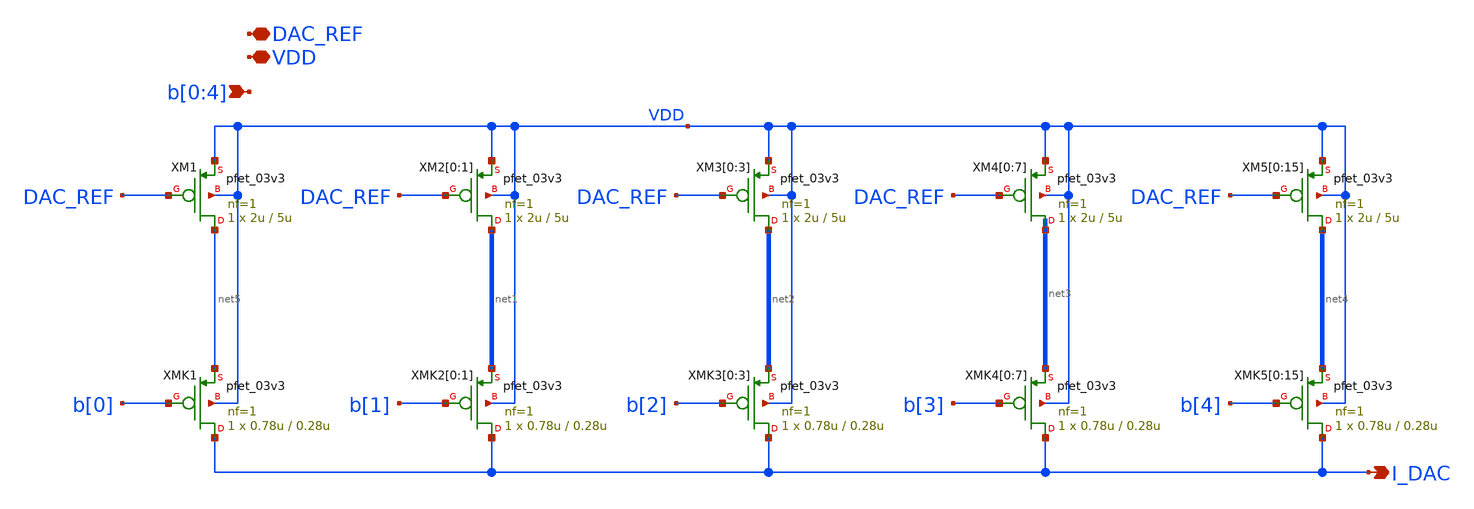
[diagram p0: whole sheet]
** sch_path: DAC_CORE_5bit/DAC_CORE_5bit.sch
**.subckt DAC_CORE_5bit I_DAC VDD DAC_REF b[0],b[1],b[2],b[3],b[4]
*.opin I_DAC
*.iopin VDD
*.iopin DAC_REF
*.ipin b[0],b[1],b[2],b[3],b[4]
XMK1 I_DAC b[0] net5 VDD pfet_03v3 L=0.28u W=0.78u nf=1 ad='int((nf+1)/2) * W/nf * 0.18u' as='int((nf+2)/2) * W/nf * 0.18u'
+ pd='2*int((nf+1)/2) * (W/nf + 0.18u)' ps='2*int((nf+2)/2) * (W/nf + 0.18u)' nrd='0.18u / W' nrs='0.18u / W'
+ sa=0 sb=0 sd=0 m=1
XMK2[0] I_DAC b[1] net1[1] VDD pfet_03v3 L=0.28u W=0.78u nf=1 ad='int((nf+1)/2) * W/nf * 0.18u' as='int((nf+2)/2) * W/nf * 0.18u'
+ pd='2*int((nf+1)/2) * (W/nf + 0.18u)' ps='2*int((nf+2)/2) * (W/nf + 0.18u)' nrd='0.18u / W' nrs='0.18u / W'
+ sa=0 sb=0 sd=0 m=1
XMK2[1] I_DAC b[1] net1[0] VDD pfet_03v3 L=0.28u W=0.78u nf=1 ad='int((nf+1)/2) * W/nf * 0.18u' as='int((nf+2)/2) * W/nf * 0.18u'
+ pd='2*int((nf+1)/2) * (W/nf + 0.18u)' ps='2*int((nf+2)/2) * (W/nf + 0.18u)' nrd='0.18u / W' nrs='0.18u / W'
+ sa=0 sb=0 sd=0 m=1
XMK3[0] I_DAC b[2] net2[3] VDD pfet_03v3 L=0.28u W=0.78u nf=1 ad='int((nf+1)/2) * W/nf * 0.18u' as='int((nf+2)/2) * W/nf * 0.18u'
+ pd='2*int((nf+1)/2) * (W/nf + 0.18u)' ps='2*int((nf+2)/2) * (W/nf + 0.18u)' nrd='0.18u / W' nrs='0.18u / W'
+ sa=0 sb=0 sd=0 m=1
XMK3[1] I_DAC b[2] net2[2] VDD pfet_03v3 L=0.28u W=0.78u nf=1 ad='int((nf+1)/2) * W/nf * 0.18u' as='int((nf+2)/2) * W/nf * 0.18u'
+ pd='2*int((nf+1)/2) * (W/nf + 0.18u)' ps='2*int((nf+2)/2) * (W/nf + 0.18u)' nrd='0.18u / W' nrs='0.18u / W'
+ sa=0 sb=0 sd=0 m=1
XMK3[2] I_DAC b[2] net2[1] VDD pfet_03v3 L=0.28u W=0.78u nf=1 ad='int((nf+1)/2) * W/nf * 0.18u' as='int((nf+2)/2) * W/nf * 0.18u'
+ pd='2*int((nf+1)/2) * (W/nf + 0.18u)' ps='2*int((nf+2)/2) * (W/nf + 0.18u)' nrd='0.18u / W' nrs='0.18u / W'
+ sa=0 sb=0 sd=0 m=1
XMK3[3] I_DAC b[2] net2[0] VDD pfet_03v3 L=0.28u W=0.78u nf=1 ad='int((nf+1)/2) * W/nf * 0.18u' as='int((nf+2)/2) * W/nf * 0.18u'
+ pd='2*int((nf+1)/2) * (W/nf + 0.18u)' ps='2*int((nf+2)/2) * (W/nf + 0.18u)' nrd='0.18u / W' nrs='0.18u / W'
+ sa=0 sb=0 sd=0 m=1
XMK4[0] I_DAC b[3] net3[7] VDD pfet_03v3 L=0.28u W=0.78u nf=1 ad='int((nf+1)/2) * W/nf * 0.18u' as='int((nf+2)/2) * W/nf * 0.18u'
+ pd='2*int((nf+1)/2) * (W/nf + 0.18u)' ps='2*int((nf+2)/2) * (W/nf + 0.18u)' nrd='0.18u / W' nrs='0.18u / W'
+ sa=0 sb=0 sd=0 m=1
XMK4[1] I_DAC b[3] net3[6] VDD pfet_03v3 L=0.28u W=0.78u nf=1 ad='int((nf+1)/2) * W/nf * 0.18u' as='int((nf+2)/2) * W/nf * 0.18u'
+ pd='2*int((nf+1)/2) * (W/nf + 0.18u)' ps='2*int((nf+2)/2) * (W/nf + 0.18u)' nrd='0.18u / W' nrs='0.18u / W'
+ sa=0 sb=0 sd=0 m=1
XMK4[2] I_DAC b[3] net3[5] VDD pfet_03v3 L=0.28u W=0.78u nf=1 ad='int((nf+1)/2) * W/nf * 0.18u' as='int((nf+2)/2) * W/nf * 0.18u'
+ pd='2*int((nf+1)/2) * (W/nf + 0.18u)' ps='2*int((nf+2)/2) * (W/nf + 0.18u)' nrd='0.18u / W' nrs='0.18u / W'
+ sa=0 sb=0 sd=0 m=1
XMK4[3] I_DAC b[3] net3[4] VDD pfet_03v3 L=0.28u W=0.78u nf=1 ad='int((nf+1)/2) * W/nf * 0.18u' as='int((nf+2)/2) * W/nf * 0.18u'
+ pd='2*int((nf+1)/2) * (W/nf + 0.18u)' ps='2*int((nf+2)/2) * (W/nf + 0.18u)' nrd='0.18u / W' nrs='0.18u / W'
+ sa=0 sb=0 sd=0 m=1
XMK4[4] I_DAC b[3] net3[3] VDD pfet_03v3 L=0.28u W=0.78u nf=1 ad='int((nf+1)/2) * W/nf * 0.18u' as='int((nf+2)/2) * W/nf * 0.18u'
+ pd='2*int((nf+1)/2) * (W/nf + 0.18u)' ps='2*int((nf+2)/2) * (W/nf + 0.18u)' nrd='0.18u / W' nrs='0.18u / W'
+ sa=0 sb=0 sd=0 m=1
XMK4[5] I_DAC b[3] net3[2] VDD pfet_03v3 L=0.28u W=0.78u nf=1 ad='int((nf+1)/2) * W/nf * 0.18u' as='int((nf+2)/2) * W/nf * 0.18u'
+ pd='2*int((nf+1)/2) * (W/nf + 0.18u)' ps='2*int((nf+2)/2) * (W/nf + 0.18u)' nrd='0.18u / W' nrs='0.18u / W'
+ sa=0 sb=0 sd=0 m=1
XMK4[6] I_DAC b[3] net3[1] VDD pfet_03v3 L=0.28u W=0.78u nf=1 ad='int((nf+1)/2) * W/nf * 0.18u' as='int((nf+2)/2) * W/nf * 0.18u'
+ pd='2*int((nf+1)/2) * (W/nf + 0.18u)' ps='2*int((nf+2)/2) * (W/nf + 0.18u)' nrd='0.18u / W' nrs='0.18u / W'
+ sa=0 sb=0 sd=0 m=1
XMK4[7] I_DAC b[3] net3[0] VDD pfet_03v3 L=0.28u W=0.78u nf=1 ad='int((nf+1)/2) * W/nf * 0.18u' as='int((nf+2)/2) * W/nf * 0.18u'
+ pd='2*int((nf+1)/2) * (W/nf + 0.18u)' ps='2*int((nf+2)/2) * (W/nf + 0.18u)' nrd='0.18u / W' nrs='0.18u / W'
+ sa=0 sb=0 sd=0 m=1
XMK5[0] I_DAC b[4] net4[15] VDD pfet_03v3 L=0.28u W=0.78u nf=1 ad='int((nf+1)/2) * W/nf * 0.18u' as='int((nf+2)/2) * W/nf * 0.18u'
+ pd='2*int((nf+1)/2) * (W/nf + 0.18u)' ps='2*int((nf+2)/2) * (W/nf + 0.18u)' nrd='0.18u / W' nrs='0.18u / W'
+ sa=0 sb=0 sd=0 m=1
XMK5[1] I_DAC b[4] net4[14] VDD pfet_03v3 L=0.28u W=0.78u nf=1 ad='int((nf+1)/2) * W/nf * 0.18u' as='int((nf+2)/2) * W/nf * 0.18u'
+ pd='2*int((nf+1)/2) * (W/nf + 0.18u)' ps='2*int((nf+2)/2) * (W/nf + 0.18u)' nrd='0.18u / W' nrs='0.18u / W'
+ sa=0 sb=0 sd=0 m=1
XMK5[2] I_DAC b[4] net4[13] VDD pfet_03v3 L=0.28u W=0.78u nf=1 ad='int((nf+1)/2) * W/nf * 0.18u' as='int((nf+2)/2) * W/nf * 0.18u'
+ pd='2*int((nf+1)/2) * (W/nf + 0.18u)' ps='2*int((nf+2)/2) * (W/nf + 0.18u)' nrd='0.18u / W' nrs='0.18u / W'
+ sa=0 sb=0 sd=0 m=1
XMK5[3] I_DAC b[4] net4[12] VDD pfet_03v3 L=0.28u W=0.78u nf=1 ad='int((nf+1)/2) * W/nf * 0.18u' as='int((nf+2)/2) * W/nf * 0.18u'
+ pd='2*int((nf+1)/2) * (W/nf + 0.18u)' ps='2*int((nf+2)/2) * (W/nf + 0.18u)' nrd='0.18u / W' nrs='0.18u / W'
+ sa=0 sb=0 sd=0 m=1
XMK5[4] I_DAC b[4] net4[11] VDD pfet_03v3 L=0.28u W=0.78u nf=1 ad='int((nf+1)/2) * W/nf * 0.18u' as='int((nf+2)/2) * W/nf * 0.18u'
+ pd='2*int((nf+1)/2) * (W/nf + 0.18u)' ps='2*int((nf+2)/2) * (W/nf + 0.18u)' nrd='0.18u / W' nrs='0.18u / W'
+ sa=0 sb=0 sd=0 m=1
XMK5[5] I_DAC b[4] net4[10] VDD pfet_03v3 L=0.28u W=0.78u nf=1 ad='int((nf+1)/2) * W/nf * 0.18u' as='int((nf+2)/2) * W/nf * 0.18u'
+ pd='2*int((nf+1)/2) * (W/nf + 0.18u)' ps='2*int((nf+2)/2) * (W/nf + 0.18u)' nrd='0.18u / W' nrs='0.18u / W'
+ sa=0 sb=0 sd=0 m=1
XMK5[6] I_DAC b[4] net4[9] VDD pfet_03v3 L=0.28u W=0.78u nf=1 ad='int((nf+1)/2) * W/nf * 0.18u' as='int((nf+2)/2) * W/nf * 0.18u'
+ pd='2*int((nf+1)/2) * (W/nf + 0.18u)' ps='2*int((nf+2)/2) * (W/nf + 0.18u)' nrd='0.18u / W' nrs='0.18u / W'
+ sa=0 sb=0 sd=0 m=1
XMK5[7] I_DAC b[4] net4[8] VDD pfet_03v3 L=0.28u W=0.78u nf=1 ad='int((nf+1)/2) * W/nf * 0.18u' as='int((nf+2)/2) * W/nf * 0.18u'
+ pd='2*int((nf+1)/2) * (W/nf + 0.18u)' ps='2*int((nf+2)/2) * (W/nf + 0.18u)' nrd='0.18u / W' nrs='0.18u / W'
+ sa=0 sb=0 sd=0 m=1
XMK5[8] I_DAC b[4] net4[7] VDD pfet_03v3 L=0.28u W=0.78u nf=1 ad='int((nf+1)/2) * W/nf * 0.18u' as='int((nf+2)/2) * W/nf * 0.18u'
+ pd='2*int((nf+1)/2) * (W/nf + 0.18u)' ps='2*int((nf+2)/2) * (W/nf + 0.18u)' nrd='0.18u / W' nrs='0.18u / W'
+ sa=0 sb=0 sd=0 m=1
XMK5[9] I_DAC b[4] net4[6] VDD pfet_03v3 L=0.28u W=0.78u nf=1 ad='int((nf+1)/2) * W/nf * 0.18u' as='int((nf+2)/2) * W/nf * 0.18u'
+ pd='2*int((nf+1)/2) * (W/nf + 0.18u)' ps='2*int((nf+2)/2) * (W/nf + 0.18u)' nrd='0.18u / W' nrs='0.18u / W'
+ sa=0 sb=0 sd=0 m=1
XMK5[10] I_DAC b[4] net4[5] VDD pfet_03v3 L=0.28u W=0.78u nf=1 ad='int((nf+1)/2) * W/nf * 0.18u' as='int((nf+2)/2) * W/nf * 0.18u'
+ pd='2*int((nf+1)/2) * (W/nf + 0.18u)' ps='2*int((nf+2)/2) * (W/nf + 0.18u)' nrd='0.18u / W' nrs='0.18u / W'
+ sa=0 sb=0 sd=0 m=1
XMK5[11] I_DAC b[4] net4[4] VDD pfet_03v3 L=0.28u W=0.78u nf=1 ad='int((nf+1)/2) * W/nf * 0.18u' as='int((nf+2)/2) * W/nf * 0.18u'
+ pd='2*int((nf+1)/2) * (W/nf + 0.18u)' ps='2*int((nf+2)/2) * (W/nf + 0.18u)' nrd='0.18u / W' nrs='0.18u / W'
+ sa=0 sb=0 sd=0 m=1
XMK5[12] I_DAC b[4] net4[3] VDD pfet_03v3 L=0.28u W=0.78u nf=1 ad='int((nf+1)/2) * W/nf * 0.18u' as='int((nf+2)/2) * W/nf * 0.18u'
+ pd='2*int((nf+1)/2) * (W/nf + 0.18u)' ps='2*int((nf+2)/2) * (W/nf + 0.18u)' nrd='0.18u / W' nrs='0.18u / W'
+ sa=0 sb=0 sd=0 m=1
XMK5[13] I_DAC b[4] net4[2] VDD pfet_03v3 L=0.28u W=0.78u nf=1 ad='int((nf+1)/2) * W/nf * 0.18u' as='int((nf+2)/2) * W/nf * 0.18u'
+ pd='2*int((nf+1)/2) * (W/nf + 0.18u)' ps='2*int((nf+2)/2) * (W/nf + 0.18u)' nrd='0.18u / W' nrs='0.18u / W'
+ sa=0 sb=0 sd=0 m=1
XMK5[14] I_DAC b[4] net4[1] VDD pfet_03v3 L=0.28u W=0.78u nf=1 ad='int((nf+1)/2) * W/nf * 0.18u' as='int((nf+2)/2) * W/nf * 0.18u'
+ pd='2*int((nf+1)/2) * (W/nf + 0.18u)' ps='2*int((nf+2)/2) * (W/nf + 0.18u)' nrd='0.18u / W' nrs='0.18u / W'
+ sa=0 sb=0 sd=0 m=1
XMK5[15] I_DAC b[4] net4[0] VDD pfet_03v3 L=0.28u W=0.78u nf=1 ad='int((nf+1)/2) * W/nf * 0.18u' as='int((nf+2)/2) * W/nf * 0.18u'
+ pd='2*int((nf+1)/2) * (W/nf + 0.18u)' ps='2*int((nf+2)/2) * (W/nf + 0.18u)' nrd='0.18u / W' nrs='0.18u / W'
+ sa=0 sb=0 sd=0 m=1
XM1 net5 DAC_REF VDD VDD pfet_03v3 L=5u W=2u nf=1 ad='int((nf+1)/2) * W/nf * 0.18u' as='int((nf+2)/2) * W/nf * 0.18u'
+ pd='2*int((nf+1)/2) * (W/nf + 0.18u)' ps='2*int((nf+2)/2) * (W/nf + 0.18u)' nrd='0.18u / W' nrs='0.18u / W'
+ sa=0 sb=0 sd=0 m=1
XM2[0] net1[1] DAC_REF VDD VDD pfet_03v3 L=5u W=2u nf=1 ad='int((nf+1)/2) * W/nf * 0.18u' as='int((nf+2)/2) * W/nf * 0.18u'
+ pd='2*int((nf+1)/2) * (W/nf + 0.18u)' ps='2*int((nf+2)/2) * (W/nf + 0.18u)' nrd='0.18u / W' nrs='0.18u / W'
+ sa=0 sb=0 sd=0 m=1
XM2[1] net1[0] DAC_REF VDD VDD pfet_03v3 L=5u W=2u nf=1 ad='int((nf+1)/2) * W/nf * 0.18u' as='int((nf+2)/2) * W/nf * 0.18u'
+ pd='2*int((nf+1)/2) * (W/nf + 0.18u)' ps='2*int((nf+2)/2) * (W/nf + 0.18u)' nrd='0.18u / W' nrs='0.18u / W'
+ sa=0 sb=0 sd=0 m=1
XM3[0] net2[3] DAC_REF VDD VDD pfet_03v3 L=5u W=2u nf=1 ad='int((nf+1)/2) * W/nf * 0.18u' as='int((nf+2)/2) * W/nf * 0.18u'
+ pd='2*int((nf+1)/2) * (W/nf + 0.18u)' ps='2*int((nf+2)/2) * (W/nf + 0.18u)' nrd='0.18u / W' nrs='0.18u / W'
+ sa=0 sb=0 sd=0 m=1
XM3[1] net2[2] DAC_REF VDD VDD pfet_03v3 L=5u W=2u nf=1 ad='int((nf+1)/2) * W/nf * 0.18u' as='int((nf+2)/2) * W/nf * 0.18u'
+ pd='2*int((nf+1)/2) * (W/nf + 0.18u)' ps='2*int((nf+2)/2) * (W/nf + 0.18u)' nrd='0.18u / W' nrs='0.18u / W'
+ sa=0 sb=0 sd=0 m=1
XM3[2] net2[1] DAC_REF VDD VDD pfet_03v3 L=5u W=2u nf=1 ad='int((nf+1)/2) * W/nf * 0.18u' as='int((nf+2)/2) * W/nf * 0.18u'
+ pd='2*int((nf+1)/2) * (W/nf + 0.18u)' ps='2*int((nf+2)/2) * (W/nf + 0.18u)' nrd='0.18u / W' nrs='0.18u / W'
+ sa=0 sb=0 sd=0 m=1
XM3[3] net2[0] DAC_REF VDD VDD pfet_03v3 L=5u W=2u nf=1 ad='int((nf+1)/2) * W/nf * 0.18u' as='int((nf+2)/2) * W/nf * 0.18u'
+ pd='2*int((nf+1)/2) * (W/nf + 0.18u)' ps='2*int((nf+2)/2) * (W/nf + 0.18u)' nrd='0.18u / W' nrs='0.18u / W'
+ sa=0 sb=0 sd=0 m=1
XM4[0] net3[7] DAC_REF VDD VDD pfet_03v3 L=5u W=2u nf=1 ad='int((nf+1)/2) * W/nf * 0.18u' as='int((nf+2)/2) * W/nf * 0.18u'
+ pd='2*int((nf+1)/2) * (W/nf + 0.18u)' ps='2*int((nf+2)/2) * (W/nf + 0.18u)' nrd='0.18u / W' nrs='0.18u / W'
+ sa=0 sb=0 sd=0 m=1
XM4[1] net3[6] DAC_REF VDD VDD pfet_03v3 L=5u W=2u nf=1 ad='int((nf+1)/2) * W/nf * 0.18u' as='int((nf+2)/2) * W/nf * 0.18u'
+ pd='2*int((nf+1)/2) * (W/nf + 0.18u)' ps='2*int((nf+2)/2) * (W/nf + 0.18u)' nrd='0.18u / W' nrs='0.18u / W'
+ sa=0 sb=0 sd=0 m=1
XM4[2] net3[5] DAC_REF VDD VDD pfet_03v3 L=5u W=2u nf=1 ad='int((nf+1)/2) * W/nf * 0.18u' as='int((nf+2)/2) * W/nf * 0.18u'
+ pd='2*int((nf+1)/2) * (W/nf + 0.18u)' ps='2*int((nf+2)/2) * (W/nf + 0.18u)' nrd='0.18u / W' nrs='0.18u / W'
+ sa=0 sb=0 sd=0 m=1
XM4[3] net3[4] DAC_REF VDD VDD pfet_03v3 L=5u W=2u nf=1 ad='int((nf+1)/2) * W/nf * 0.18u' as='int((nf+2)/2) * W/nf * 0.18u'
+ pd='2*int((nf+1)/2) * (W/nf + 0.18u)' ps='2*int((nf+2)/2) * (W/nf + 0.18u)' nrd='0.18u / W' nrs='0.18u / W'
+ sa=0 sb=0 sd=0 m=1
XM4[4] net3[3] DAC_REF VDD VDD pfet_03v3 L=5u W=2u nf=1 ad='int((nf+1)/2) * W/nf * 0.18u' as='int((nf+2)/2) * W/nf * 0.18u'
+ pd='2*int((nf+1)/2) * (W/nf + 0.18u)' ps='2*int((nf+2)/2) * (W/nf + 0.18u)' nrd='0.18u / W' nrs='0.18u / W'
+ sa=0 sb=0 sd=0 m=1
XM4[5] net3[2] DAC_REF VDD VDD pfet_03v3 L=5u W=2u nf=1 ad='int((nf+1)/2) * W/nf * 0.18u' as='int((nf+2)/2) * W/nf * 0.18u'
+ pd='2*int((nf+1)/2) * (W/nf + 0.18u)' ps='2*int((nf+2)/2) * (W/nf + 0.18u)' nrd='0.18u / W' nrs='0.18u / W'
+ sa=0 sb=0 sd=0 m=1
XM4[6] net3[1] DAC_REF VDD VDD pfet_03v3 L=5u W=2u nf=1 ad='int((nf+1)/2) * W/nf * 0.18u' as='int((nf+2)/2) * W/nf * 0.18u'
+ pd='2*int((nf+1)/2) * (W/nf + 0.18u)' ps='2*int((nf+2)/2) * (W/nf + 0.18u)' nrd='0.18u / W' nrs='0.18u / W'
+ sa=0 sb=0 sd=0 m=1
XM4[7] net3[0] DAC_REF VDD VDD pfet_03v3 L=5u W=2u nf=1 ad='int((nf+1)/2) * W/nf * 0.18u' as='int((nf+2)/2) * W/nf * 0.18u'
+ pd='2*int((nf+1)/2) * (W/nf + 0.18u)' ps='2*int((nf+2)/2) * (W/nf + 0.18u)' nrd='0.18u / W' nrs='0.18u / W'
+ sa=0 sb=0 sd=0 m=1
XM5[0] net4[15] DAC_REF VDD VDD pfet_03v3 L=5u W=2u nf=1 ad='int((nf+1)/2) * W/nf * 0.18u' as='int((nf+2)/2) * W/nf * 0.18u'
+ pd='2*int((nf+1)/2) * (W/nf + 0.18u)' ps='2*int((nf+2)/2) * (W/nf + 0.18u)' nrd='0.18u / W' nrs='0.18u / W'
+ sa=0 sb=0 sd=0 m=1
XM5[1] net4[14] DAC_REF VDD VDD pfet_03v3 L=5u W=2u nf=1 ad='int((nf+1)/2) * W/nf * 0.18u' as='int((nf+2)/2) * W/nf * 0.18u'
+ pd='2*int((nf+1)/2) * (W/nf + 0.18u)' ps='2*int((nf+2)/2) * (W/nf + 0.18u)' nrd='0.18u / W' nrs='0.18u / W'
+ sa=0 sb=0 sd=0 m=1
XM5[2] net4[13] DAC_REF VDD VDD pfet_03v3 L=5u W=2u nf=1 ad='int((nf+1)/2) * W/nf * 0.18u' as='int((nf+2)/2) * W/nf * 0.18u'
+ pd='2*int((nf+1)/2) * (W/nf + 0.18u)' ps='2*int((nf+2)/2) * (W/nf + 0.18u)' nrd='0.18u / W' nrs='0.18u / W'
+ sa=0 sb=0 sd=0 m=1
XM5[3] net4[12] DAC_REF VDD VDD pfet_03v3 L=5u W=2u nf=1 ad='int((nf+1)/2) * W/nf * 0.18u' as='int((nf+2)/2) * W/nf * 0.18u'
+ pd='2*int((nf+1)/2) * (W/nf + 0.18u)' ps='2*int((nf+2)/2) * (W/nf + 0.18u)' nrd='0.18u / W' nrs='0.18u / W'
+ sa=0 sb=0 sd=0 m=1
XM5[4] net4[11] DAC_REF VDD VDD pfet_03v3 L=5u W=2u nf=1 ad='int((nf+1)/2) * W/nf * 0.18u' as='int((nf+2)/2) * W/nf * 0.18u'
+ pd='2*int((nf+1)/2) * (W/nf + 0.18u)' ps='2*int((nf+2)/2) * (W/nf + 0.18u)' nrd='0.18u / W' nrs='0.18u / W'
+ sa=0 sb=0 sd=0 m=1
XM5[5] net4[10] DAC_REF VDD VDD pfet_03v3 L=5u W=2u nf=1 ad='int((nf+1)/2) * W/nf * 0.18u' as='int((nf+2)/2) * W/nf * 0.18u'
+ pd='2*int((nf+1)/2) * (W/nf + 0.18u)' ps='2*int((nf+2)/2) * (W/nf + 0.18u)' nrd='0.18u / W' nrs='0.18u / W'
+ sa=0 sb=0 sd=0 m=1
XM5[6] net4[9] DAC_REF VDD VDD pfet_03v3 L=5u W=2u nf=1 ad='int((nf+1)/2) * W/nf * 0.18u' as='int((nf+2)/2) * W/nf * 0.18u'
+ pd='2*int((nf+1)/2) * (W/nf + 0.18u)' ps='2*int((nf+2)/2) * (W/nf + 0.18u)' nrd='0.18u / W' nrs='0.18u / W'
+ sa=0 sb=0 sd=0 m=1
XM5[7] net4[8] DAC_REF VDD VDD pfet_03v3 L=5u W=2u nf=1 ad='int((nf+1)/2) * W/nf * 0.18u' as='int((nf+2)/2) * W/nf * 0.18u'
+ pd='2*int((nf+1)/2) * (W/nf + 0.18u)' ps='2*int((nf+2)/2) * (W/nf + 0.18u)' nrd='0.18u / W' nrs='0.18u / W'
+ sa=0 sb=0 sd=0 m=1
XM5[8] net4[7] DAC_REF VDD VDD pfet_03v3 L=5u W=2u nf=1 ad='int((nf+1)/2) * W/nf * 0.18u' as='int((nf+2)/2) * W/nf * 0.18u'
+ pd='2*int((nf+1)/2) * (W/nf + 0.18u)' ps='2*int((nf+2)/2) * (W/nf + 0.18u)' nrd='0.18u / W' nrs='0.18u / W'
+ sa=0 sb=0 sd=0 m=1
XM5[9] net4[6] DAC_REF VDD VDD pfet_03v3 L=5u W=2u nf=1 ad='int((nf+1)/2) * W/nf * 0.18u' as='int((nf+2)/2) * W/nf * 0.18u'
+ pd='2*int((nf+1)/2) * (W/nf + 0.18u)' ps='2*int((nf+2)/2) * (W/nf + 0.18u)' nrd='0.18u / W' nrs='0.18u / W'
+ sa=0 sb=0 sd=0 m=1
XM5[10] net4[5] DAC_REF VDD VDD pfet_03v3 L=5u W=2u nf=1 ad='int((nf+1)/2) * W/nf * 0.18u' as='int((nf+2)/2) * W/nf * 0.18u'
+ pd='2*int((nf+1)/2) * (W/nf + 0.18u)' ps='2*int((nf+2)/2) * (W/nf + 0.18u)' nrd='0.18u / W' nrs='0.18u / W'
+ sa=0 sb=0 sd=0 m=1
XM5[11] net4[4] DAC_REF VDD VDD pfet_03v3 L=5u W=2u nf=1 ad='int((nf+1)/2) * W/nf * 0.18u' as='int((nf+2)/2) * W/nf * 0.18u'
+ pd='2*int((nf+1)/2) * (W/nf + 0.18u)' ps='2*int((nf+2)/2) * (W/nf + 0.18u)' nrd='0.18u / W' nrs='0.18u / W'
+ sa=0 sb=0 sd=0 m=1
XM5[12] net4[3] DAC_REF VDD VDD pfet_03v3 L=5u W=2u nf=1 ad='int((nf+1)/2) * W/nf * 0.18u' as='int((nf+2)/2) * W/nf * 0.18u'
+ pd='2*int((nf+1)/2) * (W/nf + 0.18u)' ps='2*int((nf+2)/2) * (W/nf + 0.18u)' nrd='0.18u / W' nrs='0.18u / W'
+ sa=0 sb=0 sd=0 m=1
XM5[13] net4[2] DAC_REF VDD VDD pfet_03v3 L=5u W=2u nf=1 ad='int((nf+1)/2) * W/nf * 0.18u' as='int((nf+2)/2) * W/nf * 0.18u'
+ pd='2*int((nf+1)/2) * (W/nf + 0.18u)' ps='2*int((nf+2)/2) * (W/nf + 0.18u)' nrd='0.18u / W' nrs='0.18u / W'
+ sa=0 sb=0 sd=0 m=1
XM5[14] net4[1] DAC_REF VDD VDD pfet_03v3 L=5u W=2u nf=1 ad='int((nf+1)/2) * W/nf * 0.18u' as='int((nf+2)/2) * W/nf * 0.18u'
+ pd='2*int((nf+1)/2) * (W/nf + 0.18u)' ps='2*int((nf+2)/2) * (W/nf + 0.18u)' nrd='0.18u / W' nrs='0.18u / W'
+ sa=0 sb=0 sd=0 m=1
XM5[15] net4[0] DAC_REF VDD VDD pfet_03v3 L=5u W=2u nf=1 ad='int((nf+1)/2) * W/nf * 0.18u' as='int((nf+2)/2) * W/nf * 0.18u'
+ pd='2*int((nf+1)/2) * (W/nf + 0.18u)' ps='2*int((nf+2)/2) * (W/nf + 0.18u)' nrd='0.18u / W' nrs='0.18u / W'
+ sa=0 sb=0 sd=0 m=1
**.ends
.end
